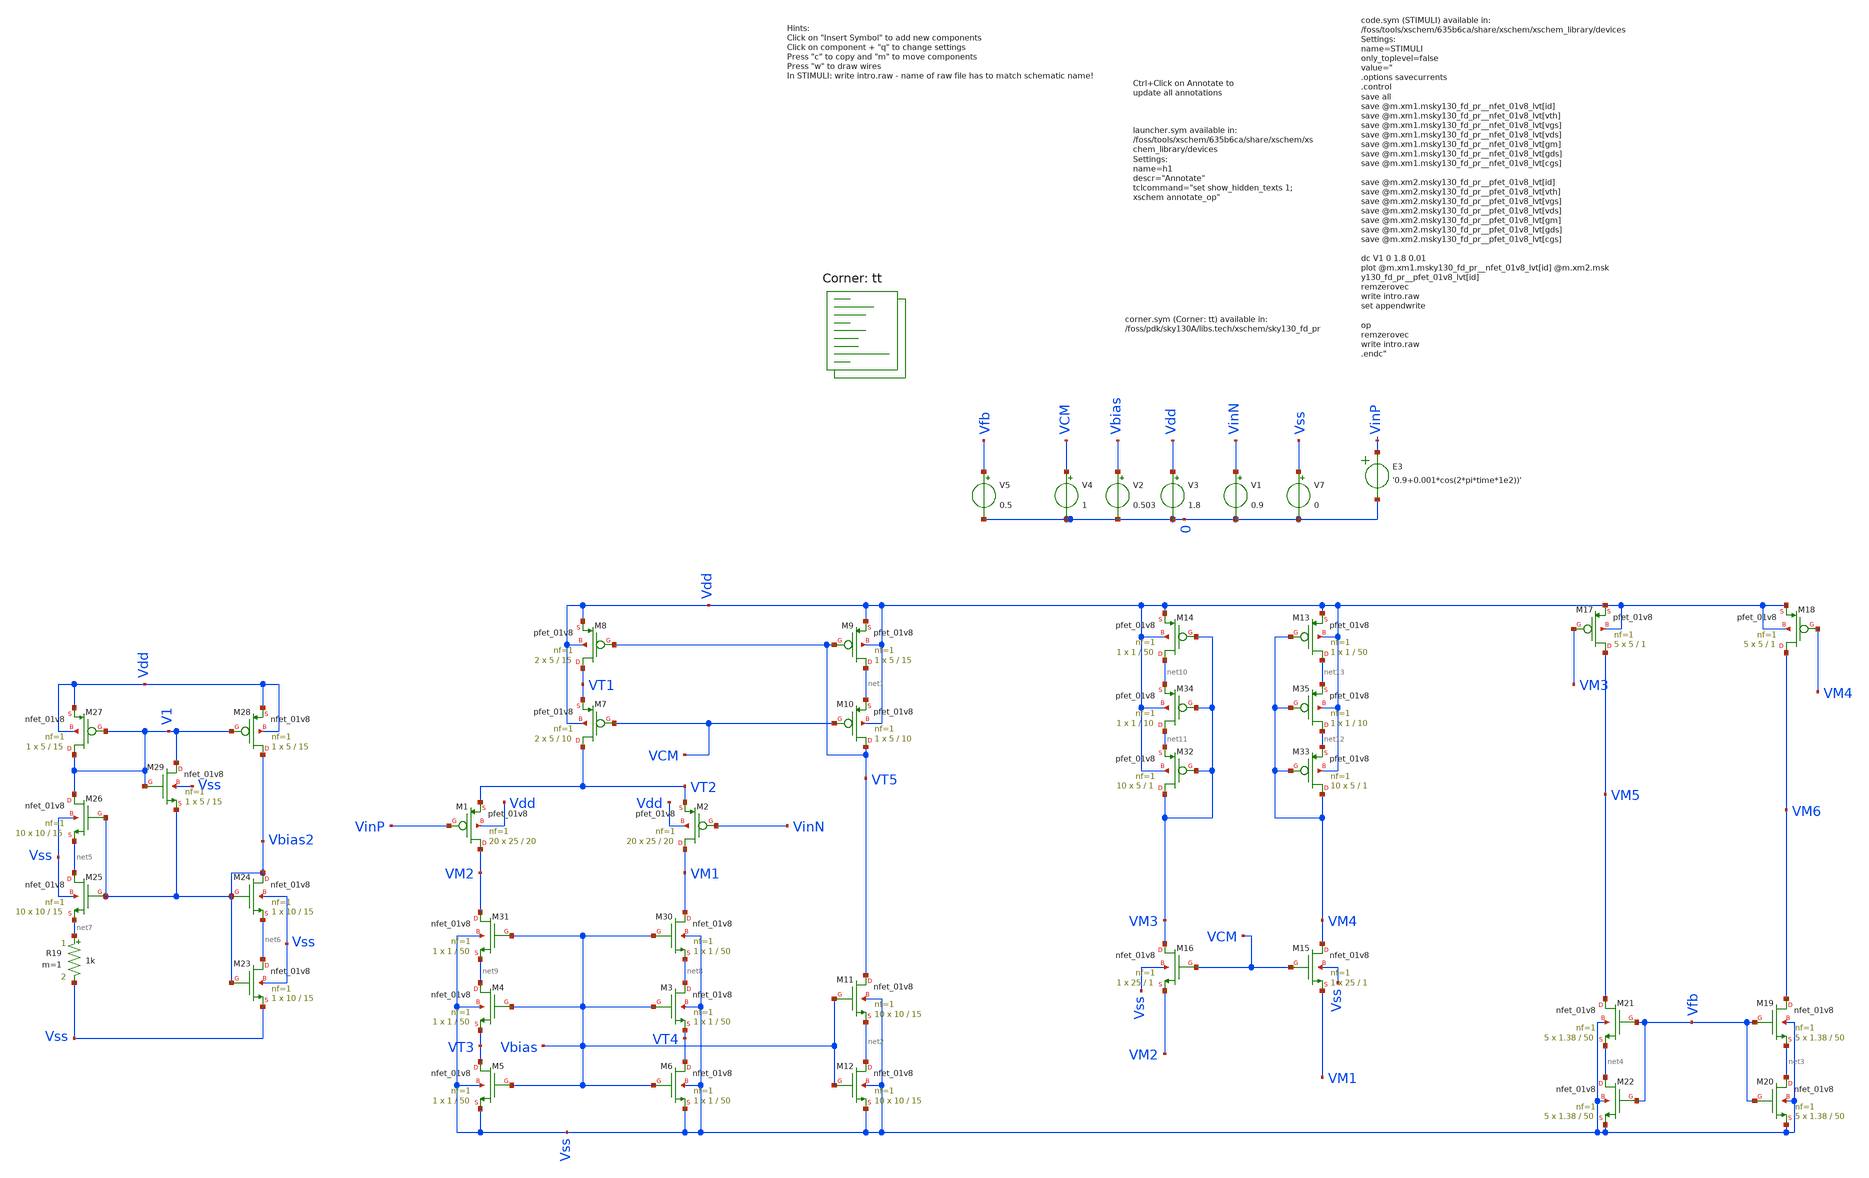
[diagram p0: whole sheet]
** sch_path: intro.sch
**.subckt intro
XM1 VM2 VinP VT2 Vdd sky130_fd_pr__pfet_01v8 L=20 W=25 nf=1 ad='int((nf+1)/2) * W/nf * 0.29' as='int((nf+2)/2) * W/nf * 0.29'
+ pd='2*int((nf+1)/2) * (W/nf + 0.29)' ps='2*int((nf+2)/2) * (W/nf + 0.29)' nrd='0.29 / W' nrs='0.29 / W'
+ sa=0 sb=0 sd=0 mult=20 m=20
XM2 VM1 VinN VT2 Vdd sky130_fd_pr__pfet_01v8 L=20 W=25 nf=1 ad='int((nf+1)/2) * W/nf * 0.29' as='int((nf+2)/2) * W/nf * 0.29'
+ pd='2*int((nf+1)/2) * (W/nf + 0.29)' ps='2*int((nf+2)/2) * (W/nf + 0.29)' nrd='0.29 / W' nrs='0.29 / W'
+ sa=0 sb=0 sd=0 mult=20 m=20
XM3 net8 Vbias VT4 Vss sky130_fd_pr__nfet_01v8 L=50 W=1 nf=1 ad='int((nf+1)/2) * W/nf * 0.29' as='int((nf+2)/2) * W/nf * 0.29'
+ pd='2*int((nf+1)/2) * (W/nf + 0.29)' ps='2*int((nf+2)/2) * (W/nf + 0.29)' nrd='0.29 / W' nrs='0.29 / W'
+ sa=0 sb=0 sd=0 mult=1 m=1
XM4 net9 Vbias VT3 Vss sky130_fd_pr__nfet_01v8 L=50 W=1 nf=1 ad='int((nf+1)/2) * W/nf * 0.29' as='int((nf+2)/2) * W/nf * 0.29'
+ pd='2*int((nf+1)/2) * (W/nf + 0.29)' ps='2*int((nf+2)/2) * (W/nf + 0.29)' nrd='0.29 / W' nrs='0.29 / W'
+ sa=0 sb=0 sd=0 mult=1 m=1
XM5 VT3 Vbias Vss Vss sky130_fd_pr__nfet_01v8 L=50 W=1 nf=1 ad='int((nf+1)/2) * W/nf * 0.29' as='int((nf+2)/2) * W/nf * 0.29'
+ pd='2*int((nf+1)/2) * (W/nf + 0.29)' ps='2*int((nf+2)/2) * (W/nf + 0.29)' nrd='0.29 / W' nrs='0.29 / W'
+ sa=0 sb=0 sd=0 mult=1 m=1
XM6 VT4 Vbias Vss Vss sky130_fd_pr__nfet_01v8 L=50 W=1 nf=1 ad='int((nf+1)/2) * W/nf * 0.29' as='int((nf+2)/2) * W/nf * 0.29'
+ pd='2*int((nf+1)/2) * (W/nf + 0.29)' ps='2*int((nf+2)/2) * (W/nf + 0.29)' nrd='0.29 / W' nrs='0.29 / W'
+ sa=0 sb=0 sd=0 mult=1 m=1
XM7 VT2 VCM VT1 Vdd sky130_fd_pr__pfet_01v8 L=10 W=5 nf=1 ad='int((nf+1)/2) * W/nf * 0.29' as='int((nf+2)/2) * W/nf * 0.29'
+ pd='2*int((nf+1)/2) * (W/nf + 0.29)' ps='2*int((nf+2)/2) * (W/nf + 0.29)' nrd='0.29 / W' nrs='0.29 / W'
+ sa=0 sb=0 sd=0 mult=2 m=2
XM8 VT1 VT5 Vdd Vdd sky130_fd_pr__pfet_01v8 L=15 W=5 nf=1 ad='int((nf+1)/2) * W/nf * 0.29' as='int((nf+2)/2) * W/nf * 0.29'
+ pd='2*int((nf+1)/2) * (W/nf + 0.29)' ps='2*int((nf+2)/2) * (W/nf + 0.29)' nrd='0.29 / W' nrs='0.29 / W'
+ sa=0 sb=0 sd=0 mult=2 m=2
XM9 net1 VT5 Vdd Vdd sky130_fd_pr__pfet_01v8 L=15 W=5 nf=1 ad='int((nf+1)/2) * W/nf * 0.29' as='int((nf+2)/2) * W/nf * 0.29'
+ pd='2*int((nf+1)/2) * (W/nf + 0.29)' ps='2*int((nf+2)/2) * (W/nf + 0.29)' nrd='0.29 / W' nrs='0.29 / W'
+ sa=0 sb=0 sd=0 mult=1 m=1
XM10 VT5 VCM net1 Vdd sky130_fd_pr__pfet_01v8 L=10 W=5 nf=1 ad='int((nf+1)/2) * W/nf * 0.29' as='int((nf+2)/2) * W/nf * 0.29'
+ pd='2*int((nf+1)/2) * (W/nf + 0.29)' ps='2*int((nf+2)/2) * (W/nf + 0.29)' nrd='0.29 / W' nrs='0.29 / W'
+ sa=0 sb=0 sd=0 mult=1 m=1
XM11 VT5 Vbias net2 Vss sky130_fd_pr__nfet_01v8 L=15 W=10 nf=1 ad='int((nf+1)/2) * W/nf * 0.29' as='int((nf+2)/2) * W/nf * 0.29'
+ pd='2*int((nf+1)/2) * (W/nf + 0.29)' ps='2*int((nf+2)/2) * (W/nf + 0.29)' nrd='0.29 / W' nrs='0.29 / W'
+ sa=0 sb=0 sd=0 mult=10 m=10
XM12 net2 Vbias Vss Vss sky130_fd_pr__nfet_01v8 L=15 W=10 nf=1 ad='int((nf+1)/2) * W/nf * 0.29' as='int((nf+2)/2) * W/nf * 0.29'
+ pd='2*int((nf+1)/2) * (W/nf + 0.29)' ps='2*int((nf+2)/2) * (W/nf + 0.29)' nrd='0.29 / W' nrs='0.29 / W'
+ sa=0 sb=0 sd=0 mult=10 m=10
XM13 net13 VM4 Vdd Vdd sky130_fd_pr__pfet_01v8 L=50 W=1 nf=1 ad='int((nf+1)/2) * W/nf * 0.29' as='int((nf+2)/2) * W/nf * 0.29'
+ pd='2*int((nf+1)/2) * (W/nf + 0.29)' ps='2*int((nf+2)/2) * (W/nf + 0.29)' nrd='0.29 / W' nrs='0.29 / W'
+ sa=0 sb=0 sd=0 mult=1 m=1
XM14 net10 VM3 Vdd Vdd sky130_fd_pr__pfet_01v8 L=50 W=1 nf=1 ad='int((nf+1)/2) * W/nf * 0.29' as='int((nf+2)/2) * W/nf * 0.29'
+ pd='2*int((nf+1)/2) * (W/nf + 0.29)' ps='2*int((nf+2)/2) * (W/nf + 0.29)' nrd='0.29 / W' nrs='0.29 / W'
+ sa=0 sb=0 sd=0 mult=1 m=1
XM15 VM4 VCM VM1 Vss sky130_fd_pr__nfet_01v8 L=1 W=25 nf=1 ad='int((nf+1)/2) * W/nf * 0.29' as='int((nf+2)/2) * W/nf * 0.29'
+ pd='2*int((nf+1)/2) * (W/nf + 0.29)' ps='2*int((nf+2)/2) * (W/nf + 0.29)' nrd='0.29 / W' nrs='0.29 / W'
+ sa=0 sb=0 sd=0 mult=1 m=1
XM16 VM3 VCM VM2 Vss sky130_fd_pr__nfet_01v8 L=1 W=25 nf=1 ad='int((nf+1)/2) * W/nf * 0.29' as='int((nf+2)/2) * W/nf * 0.29'
+ pd='2*int((nf+1)/2) * (W/nf + 0.29)' ps='2*int((nf+2)/2) * (W/nf + 0.29)' nrd='0.29 / W' nrs='0.29 / W'
+ sa=0 sb=0 sd=0 mult=1 m=1
XM17 VM5 VM3 Vdd Vdd sky130_fd_pr__pfet_01v8 L=1 W=5 nf=1 ad='int((nf+1)/2) * W/nf * 0.29' as='int((nf+2)/2) * W/nf * 0.29'
+ pd='2*int((nf+1)/2) * (W/nf + 0.29)' ps='2*int((nf+2)/2) * (W/nf + 0.29)' nrd='0.29 / W' nrs='0.29 / W'
+ sa=0 sb=0 sd=0 mult=5 m=5
XM18 VM6 VM4 Vdd Vdd sky130_fd_pr__pfet_01v8 L=1 W=5 nf=1 ad='int((nf+1)/2) * W/nf * 0.29' as='int((nf+2)/2) * W/nf * 0.29'
+ pd='2*int((nf+1)/2) * (W/nf + 0.29)' ps='2*int((nf+2)/2) * (W/nf + 0.29)' nrd='0.29 / W' nrs='0.29 / W'
+ sa=0 sb=0 sd=0 mult=5 m=5
XM19 VM6 Vfb net3 Vss sky130_fd_pr__nfet_01v8 L=50 W=1.38 nf=1 ad='int((nf+1)/2) * W/nf * 0.29' as='int((nf+2)/2) * W/nf * 0.29'
+ pd='2*int((nf+1)/2) * (W/nf + 0.29)' ps='2*int((nf+2)/2) * (W/nf + 0.29)' nrd='0.29 / W' nrs='0.29 / W'
+ sa=0 sb=0 sd=0 mult=5 m=5
XM20 net3 Vfb Vss Vss sky130_fd_pr__nfet_01v8 L=50 W=1.38 nf=1 ad='int((nf+1)/2) * W/nf * 0.29' as='int((nf+2)/2) * W/nf * 0.29'
+ pd='2*int((nf+1)/2) * (W/nf + 0.29)' ps='2*int((nf+2)/2) * (W/nf + 0.29)' nrd='0.29 / W' nrs='0.29 / W'
+ sa=0 sb=0 sd=0 mult=5 m=5
XM21 VM5 Vfb net4 Vss sky130_fd_pr__nfet_01v8 L=50 W=1.38 nf=1 ad='int((nf+1)/2) * W/nf * 0.29' as='int((nf+2)/2) * W/nf * 0.29'
+ pd='2*int((nf+1)/2) * (W/nf + 0.29)' ps='2*int((nf+2)/2) * (W/nf + 0.29)' nrd='0.29 / W' nrs='0.29 / W'
+ sa=0 sb=0 sd=0 mult=5 m=5
XM22 net4 Vfb Vss Vss sky130_fd_pr__nfet_01v8 L=50 W=1.38 nf=1 ad='int((nf+1)/2) * W/nf * 0.29' as='int((nf+2)/2) * W/nf * 0.29'
+ pd='2*int((nf+1)/2) * (W/nf + 0.29)' ps='2*int((nf+2)/2) * (W/nf + 0.29)' nrd='0.29 / W' nrs='0.29 / W'
+ sa=0 sb=0 sd=0 mult=5 m=5
E3 VinP 0 VOL=' '0.9+0.001*cos(2*pi*time*1e2))' '
V3 Vdd 0 1.8
V7 Vss 0 0
V1 VinN 0 0.9
V2 Vbias 0 0.503
V4 VCM 0 1
V5 Vfb 0 0.5
XM23 net6 Vbias2 Vss Vss sky130_fd_pr__nfet_01v8 L=15 W=10 nf=1 ad='int((nf+1)/2) * W/nf * 0.29' as='int((nf+2)/2) * W/nf * 0.29'
+ pd='2*int((nf+1)/2) * (W/nf + 0.29)' ps='2*int((nf+2)/2) * (W/nf + 0.29)' nrd='0.29 / W' nrs='0.29 / W'
+ sa=0 sb=0 sd=0 mult=1 m=1
XM24 Vbias2 Vbias2 net6 Vss sky130_fd_pr__nfet_01v8 L=15 W=10 nf=1 ad='int((nf+1)/2) * W/nf * 0.29' as='int((nf+2)/2) * W/nf * 0.29'
+ pd='2*int((nf+1)/2) * (W/nf + 0.29)' ps='2*int((nf+2)/2) * (W/nf + 0.29)' nrd='0.29 / W' nrs='0.29 / W'
+ sa=0 sb=0 sd=0 mult=1 m=1
XM25 net5 Vbias2 net7 Vss sky130_fd_pr__nfet_01v8 L=15 W=10 nf=1 ad='int((nf+1)/2) * W/nf * 0.29' as='int((nf+2)/2) * W/nf * 0.29'
+ pd='2*int((nf+1)/2) * (W/nf + 0.29)' ps='2*int((nf+2)/2) * (W/nf + 0.29)' nrd='0.29 / W' nrs='0.29 / W'
+ sa=0 sb=0 sd=0 mult=10 m=10
XM26 V1 Vbias2 net5 Vss sky130_fd_pr__nfet_01v8 L=15 W=10 nf=1 ad='int((nf+1)/2) * W/nf * 0.29' as='int((nf+2)/2) * W/nf * 0.29'
+ pd='2*int((nf+1)/2) * (W/nf + 0.29)' ps='2*int((nf+2)/2) * (W/nf + 0.29)' nrd='0.29 / W' nrs='0.29 / W'
+ sa=0 sb=0 sd=0 mult=10 m=10
XM27 V1 V1 Vdd Vdd sky130_fd_pr__nfet_01v8 L=15 W=5 nf=1 ad='int((nf+1)/2) * W/nf * 0.29' as='int((nf+2)/2) * W/nf * 0.29'
+ pd='2*int((nf+1)/2) * (W/nf + 0.29)' ps='2*int((nf+2)/2) * (W/nf + 0.29)' nrd='0.29 / W' nrs='0.29 / W'
+ sa=0 sb=0 sd=0 mult=1 m=1
XM28 Vbias2 V1 Vdd Vdd sky130_fd_pr__nfet_01v8 L=15 W=5 nf=1 ad='int((nf+1)/2) * W/nf * 0.29' as='int((nf+2)/2) * W/nf * 0.29'
+ pd='2*int((nf+1)/2) * (W/nf + 0.29)' ps='2*int((nf+2)/2) * (W/nf + 0.29)' nrd='0.29 / W' nrs='0.29 / W'
+ sa=0 sb=0 sd=0 mult=1 m=1
XM29 V1 V1 Vbias2 Vss sky130_fd_pr__nfet_01v8 L=15 W=5 nf=1 ad='int((nf+1)/2) * W/nf * 0.29' as='int((nf+2)/2) * W/nf * 0.29'
+ pd='2*int((nf+1)/2) * (W/nf + 0.29)' ps='2*int((nf+2)/2) * (W/nf + 0.29)' nrd='0.29 / W' nrs='0.29 / W'
+ sa=0 sb=0 sd=0 mult=1 m=1
R19 net7 Vss 1k m=1
XM30 VM1 Vbias net8 Vss sky130_fd_pr__nfet_01v8 L=50 W=1 nf=1 ad='int((nf+1)/2) * W/nf * 0.29' as='int((nf+2)/2) * W/nf * 0.29'
+ pd='2*int((nf+1)/2) * (W/nf + 0.29)' ps='2*int((nf+2)/2) * (W/nf + 0.29)' nrd='0.29 / W' nrs='0.29 / W'
+ sa=0 sb=0 sd=0 mult=1 m=1
XM31 VM2 Vbias net9 Vss sky130_fd_pr__nfet_01v8 L=50 W=1 nf=1 ad='int((nf+1)/2) * W/nf * 0.29' as='int((nf+2)/2) * W/nf * 0.29'
+ pd='2*int((nf+1)/2) * (W/nf + 0.29)' ps='2*int((nf+2)/2) * (W/nf + 0.29)' nrd='0.29 / W' nrs='0.29 / W'
+ sa=0 sb=0 sd=0 mult=1 m=1
XM32 VM3 VM3 net11 Vdd sky130_fd_pr__pfet_01v8 L=1 W=5 nf=1 ad='int((nf+1)/2) * W/nf * 0.29' as='int((nf+2)/2) * W/nf * 0.29'
+ pd='2*int((nf+1)/2) * (W/nf + 0.29)' ps='2*int((nf+2)/2) * (W/nf + 0.29)' nrd='0.29 / W' nrs='0.29 / W'
+ sa=0 sb=0 sd=0 mult=10 m=10
XM33 VM4 VM4 net12 Vdd sky130_fd_pr__pfet_01v8 L=1 W=5 nf=1 ad='int((nf+1)/2) * W/nf * 0.29' as='int((nf+2)/2) * W/nf * 0.29'
+ pd='2*int((nf+1)/2) * (W/nf + 0.29)' ps='2*int((nf+2)/2) * (W/nf + 0.29)' nrd='0.29 / W' nrs='0.29 / W'
+ sa=0 sb=0 sd=0 mult=10 m=10
XM34 net11 VM3 net10 Vdd sky130_fd_pr__pfet_01v8 L=10 W=1 nf=1 ad='int((nf+1)/2) * W/nf * 0.29' as='int((nf+2)/2) * W/nf * 0.29'
+ pd='2*int((nf+1)/2) * (W/nf + 0.29)' ps='2*int((nf+2)/2) * (W/nf + 0.29)' nrd='0.29 / W' nrs='0.29 / W'
+ sa=0 sb=0 sd=0 mult=1 m=1
XM35 net12 VM4 net13 Vdd sky130_fd_pr__pfet_01v8 L=10 W=1 nf=1 ad='int((nf+1)/2) * W/nf * 0.29' as='int((nf+2)/2) * W/nf * 0.29'
+ pd='2*int((nf+1)/2) * (W/nf + 0.29)' ps='2*int((nf+2)/2) * (W/nf + 0.29)' nrd='0.29 / W' nrs='0.29 / W'
+ sa=0 sb=0 sd=0 mult=1 m=1
**** begin user architecture code


.options savecurrents
.control
save all
save @m.xm1.msky130_fd_pr__nfet_01v8_lvt[id]
save @m.xm1.msky130_fd_pr__nfet_01v8_lvt[vth]
save @m.xm1.msky130_fd_pr__nfet_01v8_lvt[vgs]
save @m.xm1.msky130_fd_pr__nfet_01v8_lvt[vds]
save @m.xm1.msky130_fd_pr__nfet_01v8_lvt[gm]
save @m.xm1.msky130_fd_pr__nfet_01v8_lvt[gds]
save @m.xm1.msky130_fd_pr__nfet_01v8_lvt[cgs]

save @m.xm2.msky130_fd_pr__pfet_01v8_lvt[id]
save @m.xm2.msky130_fd_pr__pfet_01v8_lvt[vth]
save @m.xm2.msky130_fd_pr__pfet_01v8_lvt[vgs]
save @m.xm2.msky130_fd_pr__pfet_01v8_lvt[vds]
save @m.xm2.msky130_fd_pr__pfet_01v8_lvt[gm]
save @m.xm2.msky130_fd_pr__pfet_01v8_lvt[gds]
save @m.xm2.msky130_fd_pr__pfet_01v8_lvt[cgs]

*op
*remzerovec
write intro.raw
set appendwrite

*dc V1 0 1.8 0.01
*plot @m.xm1.msky130_fd_pr__nfet_01v8_lvt[id] @m.xm2.msky130_fd_pr__pfet_01v8_lvt[id]
remzerovec
write intro.raw

.endc
.tran 10u 0.01
.save all


.lib $::SKYWATER_MODELS/sky130.lib.spice tt
**** end user architecture code
**.ends
.end
